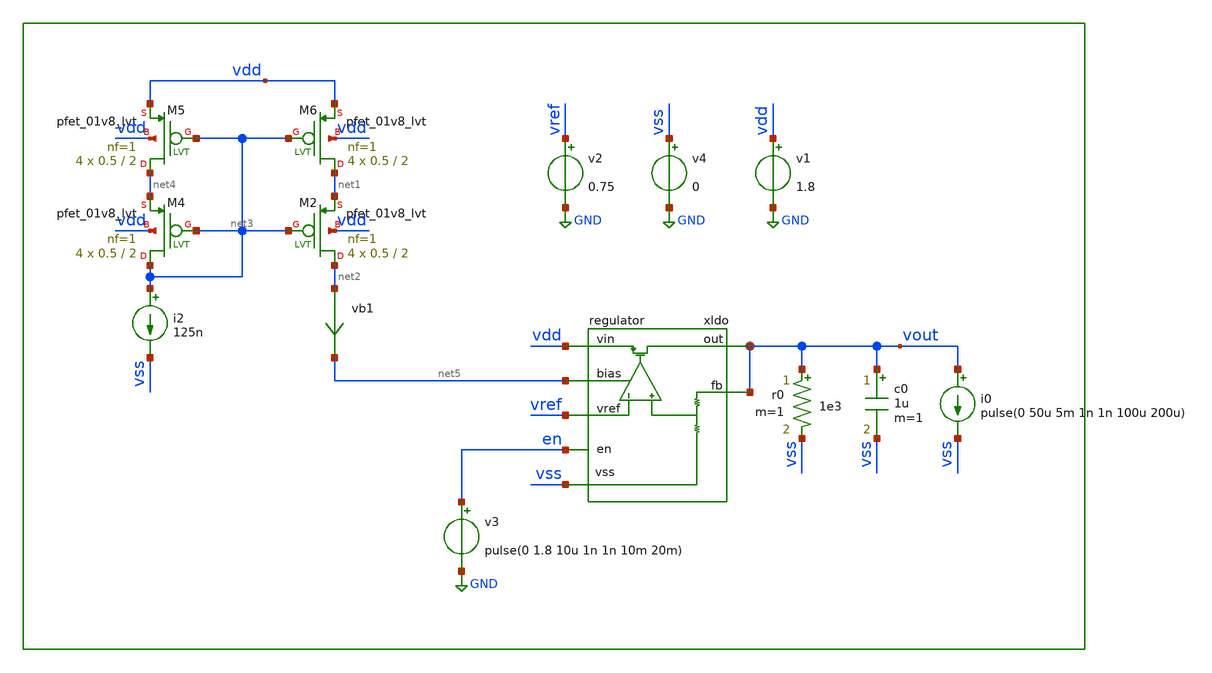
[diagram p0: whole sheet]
** sch_path: xschem/tb/regulator/tr_regulator.sch
**.subckt tr_regulator
xldo vout vref vss vdd net5 en vout regulator
vb1 net2 net5 0
.save i(vb1)
XM2 net2 net3 net1 vdd sky130_fd_pr__pfet_01v8_lvt L=2 W=0.5 nf=1 ad='int((nf+1)/2) * W/nf * 0.29' as='int((nf+2)/2) * W/nf * 0.29'
+ pd='2*int((nf+1)/2) * (W/nf + 0.29)' ps='2*int((nf+2)/2) * (W/nf + 0.29)' nrd='0.29 / W' nrs='0.29 / W'
+ sa=0 sb=0 sd=0 mult=4 m=4
XM4 net3 net3 net4 vdd sky130_fd_pr__pfet_01v8_lvt L=2 W=0.5 nf=1 ad='int((nf+1)/2) * W/nf * 0.29' as='int((nf+2)/2) * W/nf * 0.29'
+ pd='2*int((nf+1)/2) * (W/nf + 0.29)' ps='2*int((nf+2)/2) * (W/nf + 0.29)' nrd='0.29 / W' nrs='0.29 / W'
+ sa=0 sb=0 sd=0 mult=4 m=4
i2 net3 vss 125n
XM5 net4 net3 vdd vdd sky130_fd_pr__pfet_01v8_lvt L=2 W=0.5 nf=1 ad='int((nf+1)/2) * W/nf * 0.29' as='int((nf+2)/2) * W/nf * 0.29'
+ pd='2*int((nf+1)/2) * (W/nf + 0.29)' ps='2*int((nf+2)/2) * (W/nf + 0.29)' nrd='0.29 / W' nrs='0.29 / W'
+ sa=0 sb=0 sd=0 mult=4 m=4
XM6 net1 net3 vdd vdd sky130_fd_pr__pfet_01v8_lvt L=2 W=0.5 nf=1 ad='int((nf+1)/2) * W/nf * 0.29' as='int((nf+2)/2) * W/nf * 0.29'
+ pd='2*int((nf+1)/2) * (W/nf + 0.29)' ps='2*int((nf+2)/2) * (W/nf + 0.29)' nrd='0.29 / W' nrs='0.29 / W'
+ sa=0 sb=0 sd=0 mult=4 m=4
i0 vout vss pulse(0 50u 5m 1n 1n 100u 200u)
c0 vout vss 1u m=1
v2 vref GND 0.75
v1 vdd GND 1.8
v4 vss GND 0
r0 vout vss 1e3 m=1
v3 en GND pulse(0 1.8 10u 1n 1n 10m 20m)
**** begin user architecture code

.param MC_SWITCH=0

*.include $::DESIGN_PATH/regulator/regulator.sp

.control

save all
op
print all
* tran 100n 8m uic
tran 100n 1m
plt vout
.endc


* FET CORNERS
.include $::SKYWATER_MODELS/corners/tt.spice
*.include $::SKYWATER_MODELS/corners/ff.spice
*.include $::SKYWATER_MODELS/corners/ss.spice
*.include $::SKYWATER_MODELS/corners/sf.spice
*.include $::SKYWATER_MODELS/corners/fs.spice

* TT + R + C
*.include $::SKYWATER_MODELS/corners/tt_rmax_cmax.spice
*.include $::SKYWATER_MODELS/corners/tt_rmin_cmin.spice
*.include $::SKYWATER_MODELS/corners/tt_rmax_cmin.spice
*.include $::SKYWATER_MODELS/corners/tt_rmin_cmax.spice

* FF + R + C
*.include $::SKYWATER_MODELS/corners/ff_rmax_cmax.spice
*.include $::SKYWATER_MODELS/corners/ff_rmin_cmin.spice
*.include $::SKYWATER_MODELS/corners/ff_rmax_cmin.spice
*.include $::SKYWATER_MODELS/corners/ff_rmin_cmax.spice


* SS + R + C
*.include $::SKYWATER_MODELS/corners/ss_rmax_cmax.spice
*.include $::SKYWATER_MODELS/corners/ss_rmin_cmin.spice
*.include $::SKYWATER_MODELS/corners/ss_rmax_cmin.spice
*.include $::SKYWATER_MODELS/corners/ss_rmin_cmax.spice

* SF + R + C
*.include $::SKYWATER_MODELS/corners/sf_rmax_cmax.spice
*.include $::SKYWATER_MODELS/corners/sf_rmin_cmin.spice
*.include $::SKYWATER_MODELS/corners/sf_rmax_cmin.spice
*.include $::SKYWATER_MODELS/corners/sf_rmin_cmax.spice

* FS + R + C
*.include $::SKYWATER_MODELS/corners/fs_rmax_cmax.spice
*.include $::SKYWATER_MODELS/corners/fs_rmin_cmin.spice
*.include $::SKYWATER_MODELS/corners/fs_rmax_cmin.spice
*.include $::SKYWATER_MODELS/corners/fs_rmin_cmax.spice

**** end user architecture code
**.ends

* expanding   symbol:  regulator/regulator.sym # of pins=7
** sym_path: xschem/regulator/regulator.sym
** sch_path: xschem/regulator/regulator.sch
.subckt regulator out vref vss vin bias en fb
*.iopin vin
*.iopin vss
*.ipin vref
*.opin out
*.iopin bias
*.ipin en
*.ipin fb
XM2 comp vref diff vss sky130_fd_pr__nfet_01v8_lvt L=1 W=1 nf=1 ad='int((nf+1)/2) * W/nf * 0.29' as='int((nf+2)/2) * W/nf * 0.29'
+ pd='2*int((nf+1)/2) * (W/nf + 0.29)' ps='2*int((nf+2)/2) * (W/nf + 0.29)' nrd='0.29 / W' nrs='0.29 / W'
+ sa=0 sb=0 sd=0 mult=8 m=8
XM1 mirr fbdiv diff vss sky130_fd_pr__nfet_01v8_lvt L=1 W=1 nf=1 ad='int((nf+1)/2) * W/nf * 0.29' as='int((nf+2)/2) * W/nf * 0.29'
+ pd='2*int((nf+1)/2) * (W/nf + 0.29)' ps='2*int((nf+2)/2) * (W/nf + 0.29)' nrd='0.29 / W' nrs='0.29 / W'
+ sa=0 sb=0 sd=0 mult=8 m=8
XM5 diff bias vss vss sky130_fd_pr__nfet_01v8_lvt L=1 W=1 nf=1 ad='int((nf+1)/2) * W/nf * 0.29' as='int((nf+2)/2) * W/nf * 0.29'
+ pd='2*int((nf+1)/2) * (W/nf + 0.29)' ps='2*int((nf+2)/2) * (W/nf + 0.29)' nrd='0.29 / W' nrs='0.29 / W'
+ sa=0 sb=0 sd=0 mult=4 m=4
XM4 comp mirr vin vin sky130_fd_pr__pfet_01v8_lvt L=1 W=1 nf=1 ad='int((nf+1)/2) * W/nf * 0.29' as='int((nf+2)/2) * W/nf * 0.29'
+ pd='2*int((nf+1)/2) * (W/nf + 0.29)' ps='2*int((nf+2)/2) * (W/nf + 0.29)' nrd='0.29 / W' nrs='0.29 / W'
+ sa=0 sb=0 sd=0 mult=4 m=4
XM3 mirr mirr vin vin sky130_fd_pr__pfet_01v8_lvt L=1 W=1 nf=1 ad='int((nf+1)/2) * W/nf * 0.29' as='int((nf+2)/2) * W/nf * 0.29'
+ pd='2*int((nf+1)/2) * (W/nf + 0.29)' ps='2*int((nf+2)/2) * (W/nf + 0.29)' nrd='0.29 / W' nrs='0.29 / W'
+ sa=0 sb=0 sd=0 mult=4 m=4
XM6 bias bias vss vss sky130_fd_pr__nfet_01v8_lvt L=1 W=1 nf=1 ad='int((nf+1)/2) * W/nf * 0.29' as='int((nf+2)/2) * W/nf * 0.29'
+ pd='2*int((nf+1)/2) * (W/nf + 0.29)' ps='2*int((nf+2)/2) * (W/nf + 0.29)' nrd='0.29 / W' nrs='0.29 / W'
+ sa=0 sb=0 sd=0 mult=4 m=4
XM7[31] out comp vin vin sky130_fd_pr__pfet_01v8_lvt L=0.5 W=8 nf=1 ad='int((nf+1)/2) * W/nf * 0.29'
+ as='int((nf+2)/2) * W/nf * 0.29' pd='2*int((nf+1)/2) * (W/nf + 0.29)' ps='2*int((nf+2)/2) * (W/nf + 0.29)'
+ nrd='0.29 / W' nrs='0.29 / W' sa=0 sb=0 sd=0 mult=1 m=1
XM7[30] out comp vin vin sky130_fd_pr__pfet_01v8_lvt L=0.5 W=8 nf=1 ad='int((nf+1)/2) * W/nf * 0.29'
+ as='int((nf+2)/2) * W/nf * 0.29' pd='2*int((nf+1)/2) * (W/nf + 0.29)' ps='2*int((nf+2)/2) * (W/nf + 0.29)'
+ nrd='0.29 / W' nrs='0.29 / W' sa=0 sb=0 sd=0 mult=1 m=1
XM7[29] out comp vin vin sky130_fd_pr__pfet_01v8_lvt L=0.5 W=8 nf=1 ad='int((nf+1)/2) * W/nf * 0.29'
+ as='int((nf+2)/2) * W/nf * 0.29' pd='2*int((nf+1)/2) * (W/nf + 0.29)' ps='2*int((nf+2)/2) * (W/nf + 0.29)'
+ nrd='0.29 / W' nrs='0.29 / W' sa=0 sb=0 sd=0 mult=1 m=1
XM7[28] out comp vin vin sky130_fd_pr__pfet_01v8_lvt L=0.5 W=8 nf=1 ad='int((nf+1)/2) * W/nf * 0.29'
+ as='int((nf+2)/2) * W/nf * 0.29' pd='2*int((nf+1)/2) * (W/nf + 0.29)' ps='2*int((nf+2)/2) * (W/nf + 0.29)'
+ nrd='0.29 / W' nrs='0.29 / W' sa=0 sb=0 sd=0 mult=1 m=1
XM7[27] out comp vin vin sky130_fd_pr__pfet_01v8_lvt L=0.5 W=8 nf=1 ad='int((nf+1)/2) * W/nf * 0.29'
+ as='int((nf+2)/2) * W/nf * 0.29' pd='2*int((nf+1)/2) * (W/nf + 0.29)' ps='2*int((nf+2)/2) * (W/nf + 0.29)'
+ nrd='0.29 / W' nrs='0.29 / W' sa=0 sb=0 sd=0 mult=1 m=1
XM7[26] out comp vin vin sky130_fd_pr__pfet_01v8_lvt L=0.5 W=8 nf=1 ad='int((nf+1)/2) * W/nf * 0.29'
+ as='int((nf+2)/2) * W/nf * 0.29' pd='2*int((nf+1)/2) * (W/nf + 0.29)' ps='2*int((nf+2)/2) * (W/nf + 0.29)'
+ nrd='0.29 / W' nrs='0.29 / W' sa=0 sb=0 sd=0 mult=1 m=1
XM7[25] out comp vin vin sky130_fd_pr__pfet_01v8_lvt L=0.5 W=8 nf=1 ad='int((nf+1)/2) * W/nf * 0.29'
+ as='int((nf+2)/2) * W/nf * 0.29' pd='2*int((nf+1)/2) * (W/nf + 0.29)' ps='2*int((nf+2)/2) * (W/nf + 0.29)'
+ nrd='0.29 / W' nrs='0.29 / W' sa=0 sb=0 sd=0 mult=1 m=1
XM7[24] out comp vin vin sky130_fd_pr__pfet_01v8_lvt L=0.5 W=8 nf=1 ad='int((nf+1)/2) * W/nf * 0.29'
+ as='int((nf+2)/2) * W/nf * 0.29' pd='2*int((nf+1)/2) * (W/nf + 0.29)' ps='2*int((nf+2)/2) * (W/nf + 0.29)'
+ nrd='0.29 / W' nrs='0.29 / W' sa=0 sb=0 sd=0 mult=1 m=1
XM7[23] out comp vin vin sky130_fd_pr__pfet_01v8_lvt L=0.5 W=8 nf=1 ad='int((nf+1)/2) * W/nf * 0.29'
+ as='int((nf+2)/2) * W/nf * 0.29' pd='2*int((nf+1)/2) * (W/nf + 0.29)' ps='2*int((nf+2)/2) * (W/nf + 0.29)'
+ nrd='0.29 / W' nrs='0.29 / W' sa=0 sb=0 sd=0 mult=1 m=1
XM7[22] out comp vin vin sky130_fd_pr__pfet_01v8_lvt L=0.5 W=8 nf=1 ad='int((nf+1)/2) * W/nf * 0.29'
+ as='int((nf+2)/2) * W/nf * 0.29' pd='2*int((nf+1)/2) * (W/nf + 0.29)' ps='2*int((nf+2)/2) * (W/nf + 0.29)'
+ nrd='0.29 / W' nrs='0.29 / W' sa=0 sb=0 sd=0 mult=1 m=1
XM7[21] out comp vin vin sky130_fd_pr__pfet_01v8_lvt L=0.5 W=8 nf=1 ad='int((nf+1)/2) * W/nf * 0.29'
+ as='int((nf+2)/2) * W/nf * 0.29' pd='2*int((nf+1)/2) * (W/nf + 0.29)' ps='2*int((nf+2)/2) * (W/nf + 0.29)'
+ nrd='0.29 / W' nrs='0.29 / W' sa=0 sb=0 sd=0 mult=1 m=1
XM7[20] out comp vin vin sky130_fd_pr__pfet_01v8_lvt L=0.5 W=8 nf=1 ad='int((nf+1)/2) * W/nf * 0.29'
+ as='int((nf+2)/2) * W/nf * 0.29' pd='2*int((nf+1)/2) * (W/nf + 0.29)' ps='2*int((nf+2)/2) * (W/nf + 0.29)'
+ nrd='0.29 / W' nrs='0.29 / W' sa=0 sb=0 sd=0 mult=1 m=1
XM7[19] out comp vin vin sky130_fd_pr__pfet_01v8_lvt L=0.5 W=8 nf=1 ad='int((nf+1)/2) * W/nf * 0.29'
+ as='int((nf+2)/2) * W/nf * 0.29' pd='2*int((nf+1)/2) * (W/nf + 0.29)' ps='2*int((nf+2)/2) * (W/nf + 0.29)'
+ nrd='0.29 / W' nrs='0.29 / W' sa=0 sb=0 sd=0 mult=1 m=1
XM7[18] out comp vin vin sky130_fd_pr__pfet_01v8_lvt L=0.5 W=8 nf=1 ad='int((nf+1)/2) * W/nf * 0.29'
+ as='int((nf+2)/2) * W/nf * 0.29' pd='2*int((nf+1)/2) * (W/nf + 0.29)' ps='2*int((nf+2)/2) * (W/nf + 0.29)'
+ nrd='0.29 / W' nrs='0.29 / W' sa=0 sb=0 sd=0 mult=1 m=1
XM7[17] out comp vin vin sky130_fd_pr__pfet_01v8_lvt L=0.5 W=8 nf=1 ad='int((nf+1)/2) * W/nf * 0.29'
+ as='int((nf+2)/2) * W/nf * 0.29' pd='2*int((nf+1)/2) * (W/nf + 0.29)' ps='2*int((nf+2)/2) * (W/nf + 0.29)'
+ nrd='0.29 / W' nrs='0.29 / W' sa=0 sb=0 sd=0 mult=1 m=1
XM7[16] out comp vin vin sky130_fd_pr__pfet_01v8_lvt L=0.5 W=8 nf=1 ad='int((nf+1)/2) * W/nf * 0.29'
+ as='int((nf+2)/2) * W/nf * 0.29' pd='2*int((nf+1)/2) * (W/nf + 0.29)' ps='2*int((nf+2)/2) * (W/nf + 0.29)'
+ nrd='0.29 / W' nrs='0.29 / W' sa=0 sb=0 sd=0 mult=1 m=1
XM7[15] out comp vin vin sky130_fd_pr__pfet_01v8_lvt L=0.5 W=8 nf=1 ad='int((nf+1)/2) * W/nf * 0.29'
+ as='int((nf+2)/2) * W/nf * 0.29' pd='2*int((nf+1)/2) * (W/nf + 0.29)' ps='2*int((nf+2)/2) * (W/nf + 0.29)'
+ nrd='0.29 / W' nrs='0.29 / W' sa=0 sb=0 sd=0 mult=1 m=1
XM7[14] out comp vin vin sky130_fd_pr__pfet_01v8_lvt L=0.5 W=8 nf=1 ad='int((nf+1)/2) * W/nf * 0.29'
+ as='int((nf+2)/2) * W/nf * 0.29' pd='2*int((nf+1)/2) * (W/nf + 0.29)' ps='2*int((nf+2)/2) * (W/nf + 0.29)'
+ nrd='0.29 / W' nrs='0.29 / W' sa=0 sb=0 sd=0 mult=1 m=1
XM7[13] out comp vin vin sky130_fd_pr__pfet_01v8_lvt L=0.5 W=8 nf=1 ad='int((nf+1)/2) * W/nf * 0.29'
+ as='int((nf+2)/2) * W/nf * 0.29' pd='2*int((nf+1)/2) * (W/nf + 0.29)' ps='2*int((nf+2)/2) * (W/nf + 0.29)'
+ nrd='0.29 / W' nrs='0.29 / W' sa=0 sb=0 sd=0 mult=1 m=1
XM7[12] out comp vin vin sky130_fd_pr__pfet_01v8_lvt L=0.5 W=8 nf=1 ad='int((nf+1)/2) * W/nf * 0.29'
+ as='int((nf+2)/2) * W/nf * 0.29' pd='2*int((nf+1)/2) * (W/nf + 0.29)' ps='2*int((nf+2)/2) * (W/nf + 0.29)'
+ nrd='0.29 / W' nrs='0.29 / W' sa=0 sb=0 sd=0 mult=1 m=1
XM7[11] out comp vin vin sky130_fd_pr__pfet_01v8_lvt L=0.5 W=8 nf=1 ad='int((nf+1)/2) * W/nf * 0.29'
+ as='int((nf+2)/2) * W/nf * 0.29' pd='2*int((nf+1)/2) * (W/nf + 0.29)' ps='2*int((nf+2)/2) * (W/nf + 0.29)'
+ nrd='0.29 / W' nrs='0.29 / W' sa=0 sb=0 sd=0 mult=1 m=1
XM7[10] out comp vin vin sky130_fd_pr__pfet_01v8_lvt L=0.5 W=8 nf=1 ad='int((nf+1)/2) * W/nf * 0.29'
+ as='int((nf+2)/2) * W/nf * 0.29' pd='2*int((nf+1)/2) * (W/nf + 0.29)' ps='2*int((nf+2)/2) * (W/nf + 0.29)'
+ nrd='0.29 / W' nrs='0.29 / W' sa=0 sb=0 sd=0 mult=1 m=1
XM7[9] out comp vin vin sky130_fd_pr__pfet_01v8_lvt L=0.5 W=8 nf=1 ad='int((nf+1)/2) * W/nf * 0.29' as='int((nf+2)/2) * W/nf * 0.29'
+ pd='2*int((nf+1)/2) * (W/nf + 0.29)' ps='2*int((nf+2)/2) * (W/nf + 0.29)' nrd='0.29 / W' nrs='0.29 / W'
+ sa=0 sb=0 sd=0 mult=1 m=1
XM7[8] out comp vin vin sky130_fd_pr__pfet_01v8_lvt L=0.5 W=8 nf=1 ad='int((nf+1)/2) * W/nf * 0.29' as='int((nf+2)/2) * W/nf * 0.29'
+ pd='2*int((nf+1)/2) * (W/nf + 0.29)' ps='2*int((nf+2)/2) * (W/nf + 0.29)' nrd='0.29 / W' nrs='0.29 / W'
+ sa=0 sb=0 sd=0 mult=1 m=1
XM7[7] out comp vin vin sky130_fd_pr__pfet_01v8_lvt L=0.5 W=8 nf=1 ad='int((nf+1)/2) * W/nf * 0.29' as='int((nf+2)/2) * W/nf * 0.29'
+ pd='2*int((nf+1)/2) * (W/nf + 0.29)' ps='2*int((nf+2)/2) * (W/nf + 0.29)' nrd='0.29 / W' nrs='0.29 / W'
+ sa=0 sb=0 sd=0 mult=1 m=1
XM7[6] out comp vin vin sky130_fd_pr__pfet_01v8_lvt L=0.5 W=8 nf=1 ad='int((nf+1)/2) * W/nf * 0.29' as='int((nf+2)/2) * W/nf * 0.29'
+ pd='2*int((nf+1)/2) * (W/nf + 0.29)' ps='2*int((nf+2)/2) * (W/nf + 0.29)' nrd='0.29 / W' nrs='0.29 / W'
+ sa=0 sb=0 sd=0 mult=1 m=1
XM7[5] out comp vin vin sky130_fd_pr__pfet_01v8_lvt L=0.5 W=8 nf=1 ad='int((nf+1)/2) * W/nf * 0.29' as='int((nf+2)/2) * W/nf * 0.29'
+ pd='2*int((nf+1)/2) * (W/nf + 0.29)' ps='2*int((nf+2)/2) * (W/nf + 0.29)' nrd='0.29 / W' nrs='0.29 / W'
+ sa=0 sb=0 sd=0 mult=1 m=1
XM7[4] out comp vin vin sky130_fd_pr__pfet_01v8_lvt L=0.5 W=8 nf=1 ad='int((nf+1)/2) * W/nf * 0.29' as='int((nf+2)/2) * W/nf * 0.29'
+ pd='2*int((nf+1)/2) * (W/nf + 0.29)' ps='2*int((nf+2)/2) * (W/nf + 0.29)' nrd='0.29 / W' nrs='0.29 / W'
+ sa=0 sb=0 sd=0 mult=1 m=1
XM7[3] out comp vin vin sky130_fd_pr__pfet_01v8_lvt L=0.5 W=8 nf=1 ad='int((nf+1)/2) * W/nf * 0.29' as='int((nf+2)/2) * W/nf * 0.29'
+ pd='2*int((nf+1)/2) * (W/nf + 0.29)' ps='2*int((nf+2)/2) * (W/nf + 0.29)' nrd='0.29 / W' nrs='0.29 / W'
+ sa=0 sb=0 sd=0 mult=1 m=1
XM7[2] out comp vin vin sky130_fd_pr__pfet_01v8_lvt L=0.5 W=8 nf=1 ad='int((nf+1)/2) * W/nf * 0.29' as='int((nf+2)/2) * W/nf * 0.29'
+ pd='2*int((nf+1)/2) * (W/nf + 0.29)' ps='2*int((nf+2)/2) * (W/nf + 0.29)' nrd='0.29 / W' nrs='0.29 / W'
+ sa=0 sb=0 sd=0 mult=1 m=1
XM7[1] out comp vin vin sky130_fd_pr__pfet_01v8_lvt L=0.5 W=8 nf=1 ad='int((nf+1)/2) * W/nf * 0.29' as='int((nf+2)/2) * W/nf * 0.29'
+ pd='2*int((nf+1)/2) * (W/nf + 0.29)' ps='2*int((nf+2)/2) * (W/nf + 0.29)' nrd='0.29 / W' nrs='0.29 / W'
+ sa=0 sb=0 sd=0 mult=1 m=1
XM7[0] out comp vin vin sky130_fd_pr__pfet_01v8_lvt L=0.5 W=8 nf=1 ad='int((nf+1)/2) * W/nf * 0.29' as='int((nf+2)/2) * W/nf * 0.29'
+ pd='2*int((nf+1)/2) * (W/nf + 0.29)' ps='2*int((nf+2)/2) * (W/nf + 0.29)' nrd='0.29 / W' nrs='0.29 / W'
+ sa=0 sb=0 sd=0 mult=1 m=1
XC1 out comp sky130_fd_pr__cap_mim_m3_1 W=5 L=5 MF=8 m=8
XM9 bias enb vss vss sky130_fd_pr__nfet_01v8_lvt L=0.4 W=1 nf=1 ad='int((nf+1)/2) * W/nf * 0.29' as='int((nf+2)/2) * W/nf * 0.29'
+ pd='2*int((nf+1)/2) * (W/nf + 0.29)' ps='2*int((nf+2)/2) * (W/nf + 0.29)' nrd='0.29 / W' nrs='0.29 / W'
+ sa=0 sb=0 sd=0 mult=1 m=1
x1 vin en enb vss inv_lvt
XM8 comp en vin vin sky130_fd_pr__pfet_01v8_lvt L=0.4 W=1 nf=1 ad='int((nf+1)/2) * W/nf * 0.29' as='int((nf+2)/2) * W/nf * 0.29'
+ pd='2*int((nf+1)/2) * (W/nf + 0.29)' ps='2*int((nf+2)/2) * (W/nf + 0.29)' nrd='0.29 / W' nrs='0.29 / W'
+ sa=0 sb=0 sd=0 mult=1 m=1
XM10 bias bias bias vss sky130_fd_pr__nfet_01v8_lvt L=1 W=1 nf=1 ad='int((nf+1)/2) * W/nf * 0.29' as='int((nf+2)/2) * W/nf * 0.29'
+ pd='2*int((nf+1)/2) * (W/nf + 0.29)' ps='2*int((nf+2)/2) * (W/nf + 0.29)' nrd='0.29 / W' nrs='0.29 / W'
+ sa=0 sb=0 sd=0 mult=4 m=4
XM11 diff bias diff vss sky130_fd_pr__nfet_01v8_lvt L=1 W=1 nf=1 ad='int((nf+1)/2) * W/nf * 0.29' as='int((nf+2)/2) * W/nf * 0.29'
+ pd='2*int((nf+1)/2) * (W/nf + 0.29)' ps='2*int((nf+2)/2) * (W/nf + 0.29)' nrd='0.29 / W' nrs='0.29 / W'
+ sa=0 sb=0 sd=0 mult=4 m=4
XM12 comp comp comp vss sky130_fd_pr__nfet_01v8_lvt L=1 W=1 nf=1 ad='int((nf+1)/2) * W/nf * 0.29' as='int((nf+2)/2) * W/nf * 0.29'
+ pd='2*int((nf+1)/2) * (W/nf + 0.29)' ps='2*int((nf+2)/2) * (W/nf + 0.29)' nrd='0.29 / W' nrs='0.29 / W'
+ sa=0 sb=0 sd=0 mult=2 m=2
XM13 mirr mirr mirr vss sky130_fd_pr__nfet_01v8_lvt L=1 W=1 nf=1 ad='int((nf+1)/2) * W/nf * 0.29' as='int((nf+2)/2) * W/nf * 0.29'
+ pd='2*int((nf+1)/2) * (W/nf + 0.29)' ps='2*int((nf+2)/2) * (W/nf + 0.29)' nrd='0.29 / W' nrs='0.29 / W'
+ sa=0 sb=0 sd=0 mult=2 m=2
XM15 mirr mirr mirr vin sky130_fd_pr__pfet_01v8_lvt L=1 W=1 nf=1 ad='int((nf+1)/2) * W/nf * 0.29' as='int((nf+2)/2) * W/nf * 0.29'
+ pd='2*int((nf+1)/2) * (W/nf + 0.29)' ps='2*int((nf+2)/2) * (W/nf + 0.29)' nrd='0.29 / W' nrs='0.29 / W'
+ sa=0 sb=0 sd=0 mult=2 m=2
XM16 comp mirr comp vin sky130_fd_pr__pfet_01v8_lvt L=1 W=1 nf=1 ad='int((nf+1)/2) * W/nf * 0.29' as='int((nf+2)/2) * W/nf * 0.29'
+ pd='2*int((nf+1)/2) * (W/nf + 0.29)' ps='2*int((nf+2)/2) * (W/nf + 0.29)' nrd='0.29 / W' nrs='0.29 / W'
+ sa=0 sb=0 sd=0 mult=2 m=2
XR2 fbdiv fb vss sky130_fd_pr__res_xhigh_po L=34 mult=1 m=1
XR1 vss fbdiv vss sky130_fd_pr__res_xhigh_po L=34 mult=1 m=1
XR3[1] vss vss vss sky130_fd_pr__res_xhigh_po L=8.5 mult=1 m=1
XR3[0] vss vss vss sky130_fd_pr__res_xhigh_po L=8.5 mult=1 m=1
.ends


* expanding   symbol:  logic/inv_lvt.sym # of pins=4
** sym_path: xschem/logic/inv_lvt.sym
** sch_path: xschem/logic/inv_lvt.sch
.subckt inv_lvt vdd in out vss
*.iopin vdd
*.iopin vss
*.ipin in
*.opin out
XM1 out in vss vss sky130_fd_pr__nfet_01v8_lvt L=0.4 W=1 nf=1 ad='int((nf+1)/2) * W/nf * 0.29' as='int((nf+2)/2) * W/nf * 0.29'
+ pd='2*int((nf+1)/2) * (W/nf + 0.29)' ps='2*int((nf+2)/2) * (W/nf + 0.29)' nrd='0.29 / W' nrs='0.29 / W'
+ sa=0 sb=0 sd=0 mult=1 m=1
XM2 out in vdd vdd sky130_fd_pr__pfet_01v8_lvt L=0.4 W=1 nf=1 ad='int((nf+1)/2) * W/nf * 0.29' as='int((nf+2)/2) * W/nf * 0.29'
+ pd='2*int((nf+1)/2) * (W/nf + 0.29)' ps='2*int((nf+2)/2) * (W/nf + 0.29)' nrd='0.29 / W' nrs='0.29 / W'
+ sa=0 sb=0 sd=0 mult=1 m=1
.ends

.GLOBAL GND
.end
